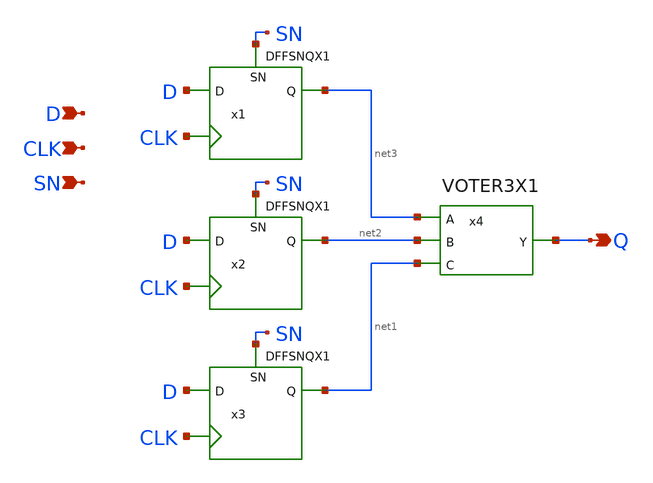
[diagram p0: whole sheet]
** sch_path: lib/xschem/TMRDFFSNQX1.sch
**.subckt TMRDFFSNQX1 Q D CLK SN
*.opin Q
*.ipin D
*.ipin CLK
*.ipin SN
x4 net3 net2 net1 Q VDD VSS VOTER3X1
x1 net3 D CLK SN VDD VSS DFFSNQX1
x2 net2 D CLK SN VDD VSS DFFSNQX1
x3 net1 D CLK SN VDD VSS DFFSNQX1
**.ends

* expanding   symbol:  VOTER3X1.sym # of pins=4
** sym_path: lib/xschem/VOTER3X1.sym
** sch_path: lib/xschem/VOTER3X1.sch
.subckt VOTER3X1 A B C Y VDD VSS
*.opin Y
*.ipin A
*.ipin B
*.ipin C
x1 Y net1 INVX1
x2 A B C net1 VDD VSS VOTERN3X1
.ends


* expanding   symbol:  VOTERN3X1.sym # of pins=4
** sym_path: VOTERN3X1.sym
** sch_path: VOTERN3X1.sch
.subckt VOTERN3X1 A B C YN VDD VSS
*.opin YN
*.ipin A
*.ipin B
*.ipin C
XM2 net1 A VDD VDD sky130_fd_pr__pfet_01v8 L=0.15 W=2 nf=1 ad='int((nf+1)/2) * W/nf * 0.29' as='int((nf+2)/2) * W/nf * 0.29'
+ pd='2*int((nf+1)/2) * (W/nf + 0.29)' ps='2*int((nf+2)/2) * (W/nf + 0.29)' nrd='0.29 / W' nrs='0.29 / W'
+ sa=0 sb=0 sd=0 mult=2 m=2
XM3 net2 B VSS VSS sky130_fd_pr__nfet_01v8 L=0.15 W=3 nf=1 ad='int((nf+1)/2) * W/nf * 0.29' as='int((nf+2)/2) * W/nf * 0.29'
+ pd='2*int((nf+1)/2) * (W/nf + 0.29)' ps='2*int((nf+2)/2) * (W/nf + 0.29)' nrd='0.29 / W' nrs='0.29 / W'
+ sa=0 sb=0 sd=0 mult=1 m=1
XM4 YN A net2 VSS sky130_fd_pr__nfet_01v8 L=0.15 W=3 nf=1 ad='int((nf+1)/2) * W/nf * 0.29' as='int((nf+2)/2) * W/nf * 0.29'
+ pd='2*int((nf+1)/2) * (W/nf + 0.29)' ps='2*int((nf+2)/2) * (W/nf + 0.29)' nrd='0.29 / W' nrs='0.29 / W'
+ sa=0 sb=0 sd=0 mult=1 m=1
XM1 net1 B VDD VDD sky130_fd_pr__pfet_01v8 L=0.15 W=2 nf=1 ad='int((nf+1)/2) * W/nf * 0.29' as='int((nf+2)/2) * W/nf * 0.29'
+ pd='2*int((nf+1)/2) * (W/nf + 0.29)' ps='2*int((nf+2)/2) * (W/nf + 0.29)' nrd='0.29 / W' nrs='0.29 / W'
+ sa=0 sb=0 sd=0 mult=2 m=2
XM5 net3 B net1 VDD sky130_fd_pr__pfet_01v8 L=0.15 W=2 nf=1 ad='int((nf+1)/2) * W/nf * 0.29' as='int((nf+2)/2) * W/nf * 0.29'
+ pd='2*int((nf+1)/2) * (W/nf + 0.29)' ps='2*int((nf+2)/2) * (W/nf + 0.29)' nrd='0.29 / W' nrs='0.29 / W'
+ sa=0 sb=0 sd=0 mult=2 m=2
XM6 YN C net3 VDD sky130_fd_pr__pfet_01v8 L=0.15 W=2 nf=1 ad='int((nf+1)/2) * W/nf * 0.29' as='int((nf+2)/2) * W/nf * 0.29'
+ pd='2*int((nf+1)/2) * (W/nf + 0.29)' ps='2*int((nf+2)/2) * (W/nf + 0.29)' nrd='0.29 / W' nrs='0.29 / W'
+ sa=0 sb=0 sd=0 mult=2 m=2
XM7 net3 C net1 VDD sky130_fd_pr__pfet_01v8 L=0.15 W=2 nf=1 ad='int((nf+1)/2) * W/nf * 0.29' as='int((nf+2)/2) * W/nf * 0.29'
+ pd='2*int((nf+1)/2) * (W/nf + 0.29)' ps='2*int((nf+2)/2) * (W/nf + 0.29)' nrd='0.29 / W' nrs='0.29 / W'
+ sa=0 sb=0 sd=0 mult=2 m=2
XM10 YN A net3 VDD sky130_fd_pr__pfet_01v8 L=0.15 W=2 nf=1 ad='int((nf+1)/2) * W/nf * 0.29' as='int((nf+2)/2) * W/nf * 0.29'
+ pd='2*int((nf+1)/2) * (W/nf + 0.29)' ps='2*int((nf+2)/2) * (W/nf + 0.29)' nrd='0.29 / W' nrs='0.29 / W'
+ sa=0 sb=0 sd=0 mult=2 m=2
XM8 net4 B VSS VSS sky130_fd_pr__nfet_01v8 L=0.15 W=3 nf=1 ad='int((nf+1)/2) * W/nf * 0.29' as='int((nf+2)/2) * W/nf * 0.29'
+ pd='2*int((nf+1)/2) * (W/nf + 0.29)' ps='2*int((nf+2)/2) * (W/nf + 0.29)' nrd='0.29 / W' nrs='0.29 / W'
+ sa=0 sb=0 sd=0 mult=1 m=1
XM9 YN C net4 VSS sky130_fd_pr__nfet_01v8 L=0.15 W=3 nf=1 ad='int((nf+1)/2) * W/nf * 0.29' as='int((nf+2)/2) * W/nf * 0.29'
+ pd='2*int((nf+1)/2) * (W/nf + 0.29)' ps='2*int((nf+2)/2) * (W/nf + 0.29)' nrd='0.29 / W' nrs='0.29 / W'
+ sa=0 sb=0 sd=0 mult=1 m=1
XM11 net5 C VSS VSS sky130_fd_pr__nfet_01v8 L=0.15 W=3 nf=1 ad='int((nf+1)/2) * W/nf * 0.29' as='int((nf+2)/2) * W/nf * 0.29'
+ pd='2*int((nf+1)/2) * (W/nf + 0.29)' ps='2*int((nf+2)/2) * (W/nf + 0.29)' nrd='0.29 / W' nrs='0.29 / W'
+ sa=0 sb=0 sd=0 mult=1 m=1
XM12 YN A net5 VSS sky130_fd_pr__nfet_01v8 L=0.15 W=3 nf=1 ad='int((nf+1)/2) * W/nf * 0.29' as='int((nf+2)/2) * W/nf * 0.29'
+ pd='2*int((nf+1)/2) * (W/nf + 0.29)' ps='2*int((nf+2)/2) * (W/nf + 0.29)' nrd='0.29 / W' nrs='0.29 / W'
+ sa=0 sb=0 sd=0 mult=1 m=1
.ends

.end
